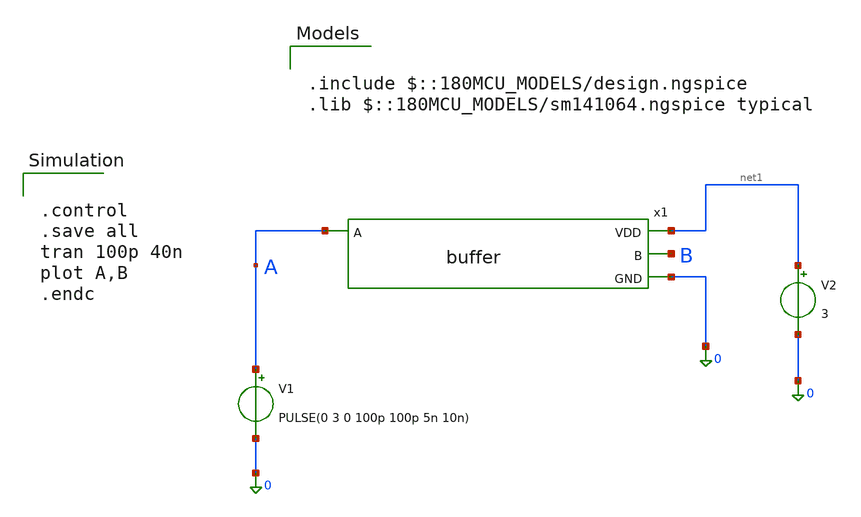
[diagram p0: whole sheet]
** sch_path: designs/libs/tb_analog/tb_buffer/tb_buffer.sch
**.subckt tb_buffer
x1 net1 A B 0 buffer
V1 A 0 PULSE(0 3 0 100p 100p 5n 10n)
V2 net1 0 3
**** begin user architecture code


.control
.save all
tran 100p 40n
plot A,B
.endc



.include $::180MCU_MODELS/design.ngspice
.lib $::180MCU_MODELS/sm141064.ngspice typical

**** end user architecture code
**.ends

* expanding   symbol:  buffer.sym # of pins=4
** sym_path: designs/libs/tb_analog/tb_buffer/buffer.sym
** sch_path: designs/libs/tb_analog/tb_buffer/buffer.sch
.subckt buffer VDD A B GND
*.ipin A
*.opin VDD
*.opin GND
*.opin B
x1 VDD A net1 GND inv
x2 VDD net1 B GND inv
.ends


* expanding   symbol:  inv.sym # of pins=4
** sym_path: designs/libs/tb_analog/tb_inv/inv.sym
** sch_path: designs/libs/tb_analog/tb_inv/inv.sch
.subckt inv VDD A B GND
*.ipin A
*.opin B
*.iopin VDD
*.iopin GND
XM1 B A GND GND nfet_05v0 L=0.70u W=2u nf=1 ad='int((nf+1)/2) * W/nf * 0.18u' as='int((nf+2)/2) * W/nf * 0.18u'
+ pd='2*int((nf+1)/2) * (W/nf + 0.18u)' ps='2*int((nf+2)/2) * (W/nf + 0.18u)' nrd='0.18u / W' nrs='0.18u / W'
+ sa=0 sb=0 sd=0 m=1
XM2 B A VDD VDD pfet_05v0 L=0.7u W=5u nf=1 ad='int((nf+1)/2) * W/nf * 0.18u' as='int((nf+2)/2) * W/nf * 0.18u'
+ pd='2*int((nf+1)/2) * (W/nf + 0.18u)' ps='2*int((nf+2)/2) * (W/nf + 0.18u)' nrd='0.18u / W' nrs='0.18u / W'
+ sa=0 sb=0 sd=0 m=1
.ends

.end
